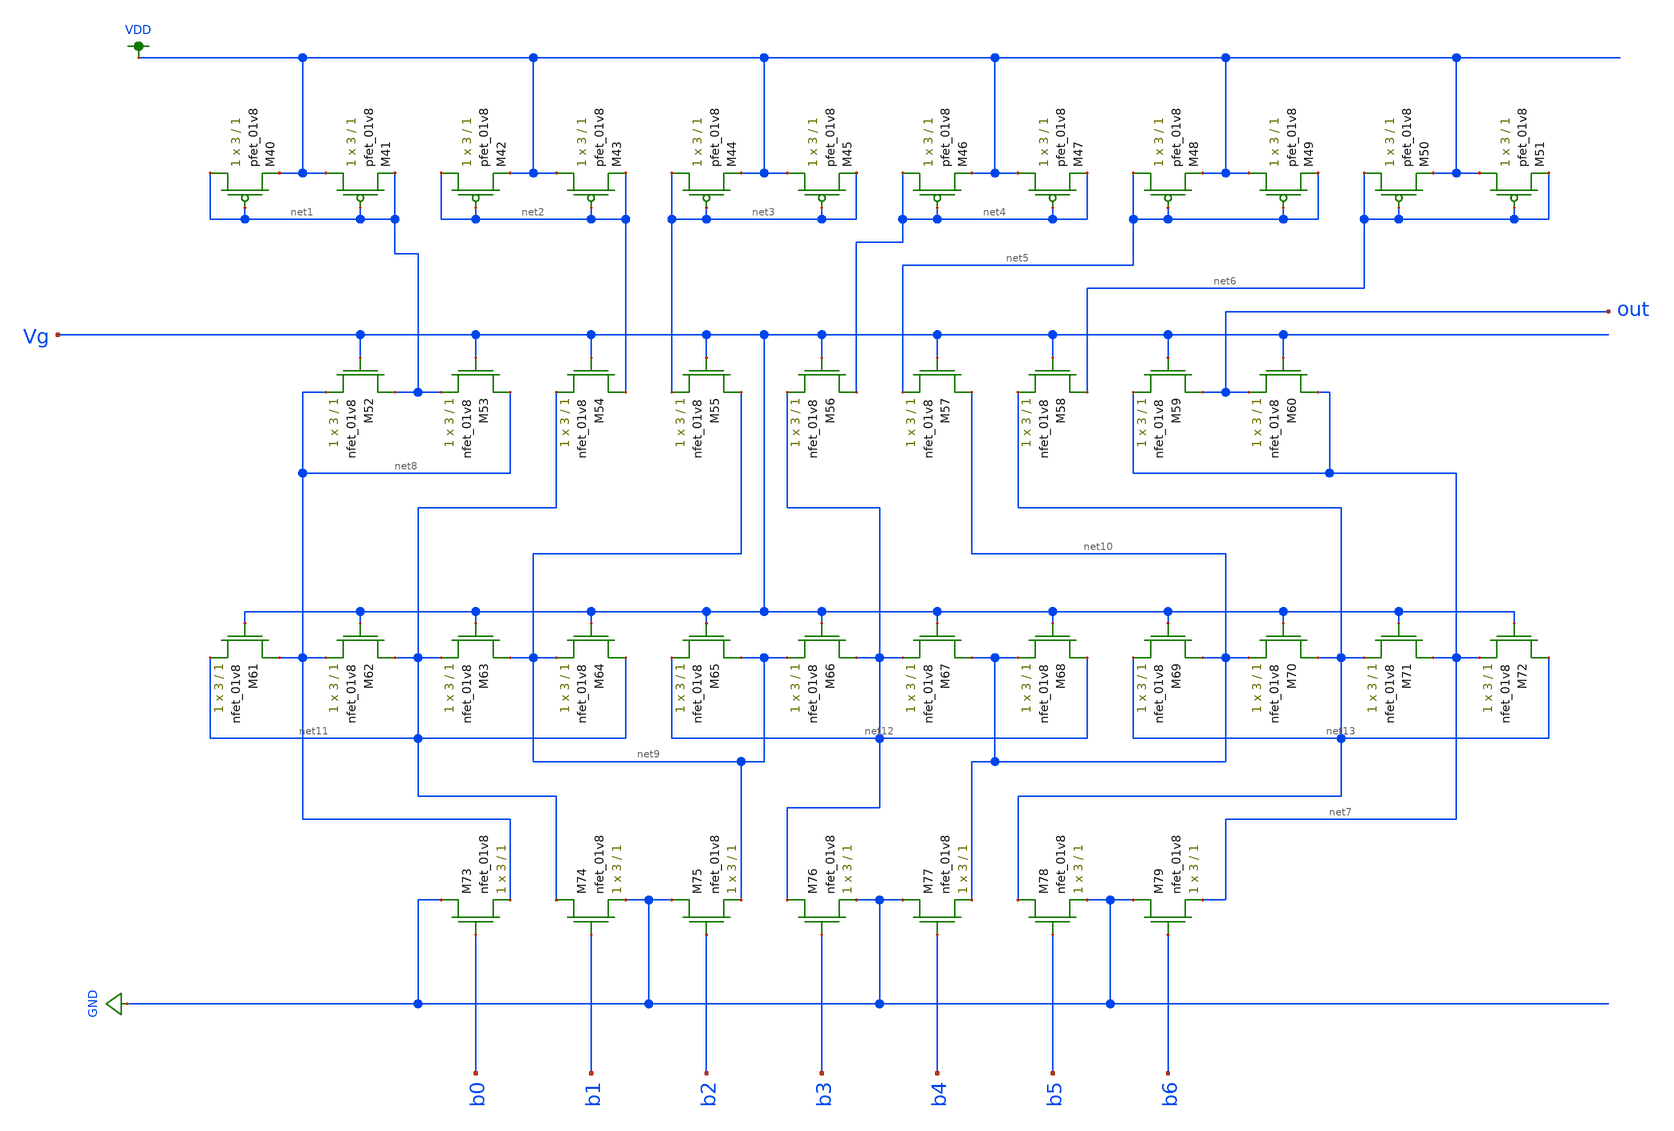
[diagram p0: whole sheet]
** sch_path: schematic/LDS/dac_7_bit_LDS.sch
**.subckt dac_7_bit_LDS
XM40 net1 net1 VDD VDD sky130_fd_pr__pfet_01v8 L=1 W=3 nf=1 ad='int((nf+1)/2) * W/nf * 0.29' as='int((nf+2)/2) * W/nf * 0.29'
+ pd='2*int((nf+1)/2) * (W/nf + 0.29)' ps='2*int((nf+2)/2) * (W/nf + 0.29)' nrd='0.29 / W' nrs='0.29 / W'
+ sa=0 sb=0 sd=0 mult=1 m=1
XM41 VDD net1 net1 VDD sky130_fd_pr__pfet_01v8 L=1 W=3 nf=1 ad='int((nf+1)/2) * W/nf * 0.29' as='int((nf+2)/2) * W/nf * 0.29'
+ pd='2*int((nf+1)/2) * (W/nf + 0.29)' ps='2*int((nf+2)/2) * (W/nf + 0.29)' nrd='0.29 / W' nrs='0.29 / W'
+ sa=0 sb=0 sd=0 mult=1 m=1
XM42 net2 net2 VDD VDD sky130_fd_pr__pfet_01v8 L=1 W=3 nf=1 ad='int((nf+1)/2) * W/nf * 0.29' as='int((nf+2)/2) * W/nf * 0.29'
+ pd='2*int((nf+1)/2) * (W/nf + 0.29)' ps='2*int((nf+2)/2) * (W/nf + 0.29)' nrd='0.29 / W' nrs='0.29 / W'
+ sa=0 sb=0 sd=0 mult=1 m=1
XM43 VDD net2 net2 VDD sky130_fd_pr__pfet_01v8 L=1 W=3 nf=1 ad='int((nf+1)/2) * W/nf * 0.29' as='int((nf+2)/2) * W/nf * 0.29'
+ pd='2*int((nf+1)/2) * (W/nf + 0.29)' ps='2*int((nf+2)/2) * (W/nf + 0.29)' nrd='0.29 / W' nrs='0.29 / W'
+ sa=0 sb=0 sd=0 mult=1 m=1
XM44 net3 net3 VDD VDD sky130_fd_pr__pfet_01v8 L=1 W=3 nf=1 ad='int((nf+1)/2) * W/nf * 0.29' as='int((nf+2)/2) * W/nf * 0.29'
+ pd='2*int((nf+1)/2) * (W/nf + 0.29)' ps='2*int((nf+2)/2) * (W/nf + 0.29)' nrd='0.29 / W' nrs='0.29 / W'
+ sa=0 sb=0 sd=0 mult=1 m=1
XM45 VDD net3 net3 VDD sky130_fd_pr__pfet_01v8 L=1 W=3 nf=1 ad='int((nf+1)/2) * W/nf * 0.29' as='int((nf+2)/2) * W/nf * 0.29'
+ pd='2*int((nf+1)/2) * (W/nf + 0.29)' ps='2*int((nf+2)/2) * (W/nf + 0.29)' nrd='0.29 / W' nrs='0.29 / W'
+ sa=0 sb=0 sd=0 mult=1 m=1
XM46 net4 net4 VDD VDD sky130_fd_pr__pfet_01v8 L=1 W=3 nf=1 ad='int((nf+1)/2) * W/nf * 0.29' as='int((nf+2)/2) * W/nf * 0.29'
+ pd='2*int((nf+1)/2) * (W/nf + 0.29)' ps='2*int((nf+2)/2) * (W/nf + 0.29)' nrd='0.29 / W' nrs='0.29 / W'
+ sa=0 sb=0 sd=0 mult=1 m=1
XM47 VDD net4 net4 VDD sky130_fd_pr__pfet_01v8 L=1 W=3 nf=1 ad='int((nf+1)/2) * W/nf * 0.29' as='int((nf+2)/2) * W/nf * 0.29'
+ pd='2*int((nf+1)/2) * (W/nf + 0.29)' ps='2*int((nf+2)/2) * (W/nf + 0.29)' nrd='0.29 / W' nrs='0.29 / W'
+ sa=0 sb=0 sd=0 mult=1 m=1
XM48 net5 net5 VDD VDD sky130_fd_pr__pfet_01v8 L=1 W=3 nf=1 ad='int((nf+1)/2) * W/nf * 0.29' as='int((nf+2)/2) * W/nf * 0.29'
+ pd='2*int((nf+1)/2) * (W/nf + 0.29)' ps='2*int((nf+2)/2) * (W/nf + 0.29)' nrd='0.29 / W' nrs='0.29 / W'
+ sa=0 sb=0 sd=0 mult=1 m=1
XM49 VDD net5 net5 VDD sky130_fd_pr__pfet_01v8 L=1 W=3 nf=1 ad='int((nf+1)/2) * W/nf * 0.29' as='int((nf+2)/2) * W/nf * 0.29'
+ pd='2*int((nf+1)/2) * (W/nf + 0.29)' ps='2*int((nf+2)/2) * (W/nf + 0.29)' nrd='0.29 / W' nrs='0.29 / W'
+ sa=0 sb=0 sd=0 mult=1 m=1
XM50 net6 net6 VDD VDD sky130_fd_pr__pfet_01v8 L=1 W=3 nf=1 ad='int((nf+1)/2) * W/nf * 0.29' as='int((nf+2)/2) * W/nf * 0.29'
+ pd='2*int((nf+1)/2) * (W/nf + 0.29)' ps='2*int((nf+2)/2) * (W/nf + 0.29)' nrd='0.29 / W' nrs='0.29 / W'
+ sa=0 sb=0 sd=0 mult=1 m=1
XM51 VDD net6 net6 VDD sky130_fd_pr__pfet_01v8 L=1 W=3 nf=1 ad='int((nf+1)/2) * W/nf * 0.29' as='int((nf+2)/2) * W/nf * 0.29'
+ pd='2*int((nf+1)/2) * (W/nf + 0.29)' ps='2*int((nf+2)/2) * (W/nf + 0.29)' nrd='0.29 / W' nrs='0.29 / W'
+ sa=0 sb=0 sd=0 mult=1 m=1
XM52 net1 Vg net8 GND sky130_fd_pr__nfet_01v8 L=1 W=3 nf=1 ad='int((nf+1)/2) * W/nf * 0.29' as='int((nf+2)/2) * W/nf * 0.29'
+ pd='2*int((nf+1)/2) * (W/nf + 0.29)' ps='2*int((nf+2)/2) * (W/nf + 0.29)' nrd='0.29 / W' nrs='0.29 / W'
+ sa=0 sb=0 sd=0 mult=1 m=1
XM53 net8 Vg net1 GND sky130_fd_pr__nfet_01v8 L=1 W=3 nf=1 ad='int((nf+1)/2) * W/nf * 0.29' as='int((nf+2)/2) * W/nf * 0.29'
+ pd='2*int((nf+1)/2) * (W/nf + 0.29)' ps='2*int((nf+2)/2) * (W/nf + 0.29)' nrd='0.29 / W' nrs='0.29 / W'
+ sa=0 sb=0 sd=0 mult=1 m=1
XM54 net2 Vg net11 GND sky130_fd_pr__nfet_01v8 L=1 W=3 nf=1 ad='int((nf+1)/2) * W/nf * 0.29' as='int((nf+2)/2) * W/nf * 0.29'
+ pd='2*int((nf+1)/2) * (W/nf + 0.29)' ps='2*int((nf+2)/2) * (W/nf + 0.29)' nrd='0.29 / W' nrs='0.29 / W'
+ sa=0 sb=0 sd=0 mult=1 m=1
XM55 net9 Vg net3 GND sky130_fd_pr__nfet_01v8 L=1 W=3 nf=1 ad='int((nf+1)/2) * W/nf * 0.29' as='int((nf+2)/2) * W/nf * 0.29'
+ pd='2*int((nf+1)/2) * (W/nf + 0.29)' ps='2*int((nf+2)/2) * (W/nf + 0.29)' nrd='0.29 / W' nrs='0.29 / W'
+ sa=0 sb=0 sd=0 mult=1 m=1
XM56 net4 Vg net12 GND sky130_fd_pr__nfet_01v8 L=1 W=3 nf=1 ad='int((nf+1)/2) * W/nf * 0.29' as='int((nf+2)/2) * W/nf * 0.29'
+ pd='2*int((nf+1)/2) * (W/nf + 0.29)' ps='2*int((nf+2)/2) * (W/nf + 0.29)' nrd='0.29 / W' nrs='0.29 / W'
+ sa=0 sb=0 sd=0 mult=1 m=1
XM57 net10 Vg net5 GND sky130_fd_pr__nfet_01v8 L=1 W=3 nf=1 ad='int((nf+1)/2) * W/nf * 0.29' as='int((nf+2)/2) * W/nf * 0.29'
+ pd='2*int((nf+1)/2) * (W/nf + 0.29)' ps='2*int((nf+2)/2) * (W/nf + 0.29)' nrd='0.29 / W' nrs='0.29 / W'
+ sa=0 sb=0 sd=0 mult=1 m=1
XM58 net6 Vg net13 GND sky130_fd_pr__nfet_01v8 L=1 W=3 nf=1 ad='int((nf+1)/2) * W/nf * 0.29' as='int((nf+2)/2) * W/nf * 0.29'
+ pd='2*int((nf+1)/2) * (W/nf + 0.29)' ps='2*int((nf+2)/2) * (W/nf + 0.29)' nrd='0.29 / W' nrs='0.29 / W'
+ sa=0 sb=0 sd=0 mult=1 m=1
XM59 out Vg net7 GND sky130_fd_pr__nfet_01v8 L=1 W=3 nf=1 ad='int((nf+1)/2) * W/nf * 0.29' as='int((nf+2)/2) * W/nf * 0.29'
+ pd='2*int((nf+1)/2) * (W/nf + 0.29)' ps='2*int((nf+2)/2) * (W/nf + 0.29)' nrd='0.29 / W' nrs='0.29 / W'
+ sa=0 sb=0 sd=0 mult=1 m=1
XM60 net7 Vg out GND sky130_fd_pr__nfet_01v8 L=1 W=3 nf=1 ad='int((nf+1)/2) * W/nf * 0.29' as='int((nf+2)/2) * W/nf * 0.29'
+ pd='2*int((nf+1)/2) * (W/nf + 0.29)' ps='2*int((nf+2)/2) * (W/nf + 0.29)' nrd='0.29 / W' nrs='0.29 / W'
+ sa=0 sb=0 sd=0 mult=1 m=1
XM61 net8 Vg net11 GND sky130_fd_pr__nfet_01v8 L=1 W=3 nf=1 ad='int((nf+1)/2) * W/nf * 0.29' as='int((nf+2)/2) * W/nf * 0.29'
+ pd='2*int((nf+1)/2) * (W/nf + 0.29)' ps='2*int((nf+2)/2) * (W/nf + 0.29)' nrd='0.29 / W' nrs='0.29 / W'
+ sa=0 sb=0 sd=0 mult=1 m=1
XM62 net11 Vg net8 GND sky130_fd_pr__nfet_01v8 L=1 W=3 nf=1 ad='int((nf+1)/2) * W/nf * 0.29' as='int((nf+2)/2) * W/nf * 0.29'
+ pd='2*int((nf+1)/2) * (W/nf + 0.29)' ps='2*int((nf+2)/2) * (W/nf + 0.29)' nrd='0.29 / W' nrs='0.29 / W'
+ sa=0 sb=0 sd=0 mult=1 m=1
XM63 net9 Vg net11 GND sky130_fd_pr__nfet_01v8 L=1 W=3 nf=1 ad='int((nf+1)/2) * W/nf * 0.29' as='int((nf+2)/2) * W/nf * 0.29'
+ pd='2*int((nf+1)/2) * (W/nf + 0.29)' ps='2*int((nf+2)/2) * (W/nf + 0.29)' nrd='0.29 / W' nrs='0.29 / W'
+ sa=0 sb=0 sd=0 mult=1 m=1
XM64 net11 Vg net9 GND sky130_fd_pr__nfet_01v8 L=1 W=3 nf=1 ad='int((nf+1)/2) * W/nf * 0.29' as='int((nf+2)/2) * W/nf * 0.29'
+ pd='2*int((nf+1)/2) * (W/nf + 0.29)' ps='2*int((nf+2)/2) * (W/nf + 0.29)' nrd='0.29 / W' nrs='0.29 / W'
+ sa=0 sb=0 sd=0 mult=1 m=1
XM65 net9 Vg net12 GND sky130_fd_pr__nfet_01v8 L=1 W=3 nf=1 ad='int((nf+1)/2) * W/nf * 0.29' as='int((nf+2)/2) * W/nf * 0.29'
+ pd='2*int((nf+1)/2) * (W/nf + 0.29)' ps='2*int((nf+2)/2) * (W/nf + 0.29)' nrd='0.29 / W' nrs='0.29 / W'
+ sa=0 sb=0 sd=0 mult=1 m=1
XM66 net12 Vg net9 GND sky130_fd_pr__nfet_01v8 L=1 W=3 nf=1 ad='int((nf+1)/2) * W/nf * 0.29' as='int((nf+2)/2) * W/nf * 0.29'
+ pd='2*int((nf+1)/2) * (W/nf + 0.29)' ps='2*int((nf+2)/2) * (W/nf + 0.29)' nrd='0.29 / W' nrs='0.29 / W'
+ sa=0 sb=0 sd=0 mult=1 m=1
XM67 net10 Vg net12 GND sky130_fd_pr__nfet_01v8 L=1 W=3 nf=1 ad='int((nf+1)/2) * W/nf * 0.29' as='int((nf+2)/2) * W/nf * 0.29'
+ pd='2*int((nf+1)/2) * (W/nf + 0.29)' ps='2*int((nf+2)/2) * (W/nf + 0.29)' nrd='0.29 / W' nrs='0.29 / W'
+ sa=0 sb=0 sd=0 mult=1 m=1
XM68 net12 Vg net10 GND sky130_fd_pr__nfet_01v8 L=1 W=3 nf=1 ad='int((nf+1)/2) * W/nf * 0.29' as='int((nf+2)/2) * W/nf * 0.29'
+ pd='2*int((nf+1)/2) * (W/nf + 0.29)' ps='2*int((nf+2)/2) * (W/nf + 0.29)' nrd='0.29 / W' nrs='0.29 / W'
+ sa=0 sb=0 sd=0 mult=1 m=1
XM69 net10 Vg net13 GND sky130_fd_pr__nfet_01v8 L=1 W=3 nf=1 ad='int((nf+1)/2) * W/nf * 0.29' as='int((nf+2)/2) * W/nf * 0.29'
+ pd='2*int((nf+1)/2) * (W/nf + 0.29)' ps='2*int((nf+2)/2) * (W/nf + 0.29)' nrd='0.29 / W' nrs='0.29 / W'
+ sa=0 sb=0 sd=0 mult=1 m=1
XM70 net13 Vg net10 GND sky130_fd_pr__nfet_01v8 L=1 W=3 nf=1 ad='int((nf+1)/2) * W/nf * 0.29' as='int((nf+2)/2) * W/nf * 0.29'
+ pd='2*int((nf+1)/2) * (W/nf + 0.29)' ps='2*int((nf+2)/2) * (W/nf + 0.29)' nrd='0.29 / W' nrs='0.29 / W'
+ sa=0 sb=0 sd=0 mult=1 m=1
XM71 net7 Vg net13 GND sky130_fd_pr__nfet_01v8 L=1 W=3 nf=1 ad='int((nf+1)/2) * W/nf * 0.29' as='int((nf+2)/2) * W/nf * 0.29'
+ pd='2*int((nf+1)/2) * (W/nf + 0.29)' ps='2*int((nf+2)/2) * (W/nf + 0.29)' nrd='0.29 / W' nrs='0.29 / W'
+ sa=0 sb=0 sd=0 mult=1 m=1
XM72 net13 Vg net7 GND sky130_fd_pr__nfet_01v8 L=1 W=3 nf=1 ad='int((nf+1)/2) * W/nf * 0.29' as='int((nf+2)/2) * W/nf * 0.29'
+ pd='2*int((nf+1)/2) * (W/nf + 0.29)' ps='2*int((nf+2)/2) * (W/nf + 0.29)' nrd='0.29 / W' nrs='0.29 / W'
+ sa=0 sb=0 sd=0 mult=1 m=1
XM73 GND b0 net8 GND sky130_fd_pr__nfet_01v8 L=1 W=3 nf=1 ad='int((nf+1)/2) * W/nf * 0.29' as='int((nf+2)/2) * W/nf * 0.29'
+ pd='2*int((nf+1)/2) * (W/nf + 0.29)' ps='2*int((nf+2)/2) * (W/nf + 0.29)' nrd='0.29 / W' nrs='0.29 / W'
+ sa=0 sb=0 sd=0 mult=1 m=1
XM74 net11 b1 GND GND sky130_fd_pr__nfet_01v8 L=1 W=3 nf=1 ad='int((nf+1)/2) * W/nf * 0.29' as='int((nf+2)/2) * W/nf * 0.29'
+ pd='2*int((nf+1)/2) * (W/nf + 0.29)' ps='2*int((nf+2)/2) * (W/nf + 0.29)' nrd='0.29 / W' nrs='0.29 / W'
+ sa=0 sb=0 sd=0 mult=1 m=1
XM75 GND b2 net9 GND sky130_fd_pr__nfet_01v8 L=1 W=3 nf=1 ad='int((nf+1)/2) * W/nf * 0.29' as='int((nf+2)/2) * W/nf * 0.29'
+ pd='2*int((nf+1)/2) * (W/nf + 0.29)' ps='2*int((nf+2)/2) * (W/nf + 0.29)' nrd='0.29 / W' nrs='0.29 / W'
+ sa=0 sb=0 sd=0 mult=1 m=1
XM76 net12 b3 GND GND sky130_fd_pr__nfet_01v8 L=1 W=3 nf=1 ad='int((nf+1)/2) * W/nf * 0.29' as='int((nf+2)/2) * W/nf * 0.29'
+ pd='2*int((nf+1)/2) * (W/nf + 0.29)' ps='2*int((nf+2)/2) * (W/nf + 0.29)' nrd='0.29 / W' nrs='0.29 / W'
+ sa=0 sb=0 sd=0 mult=1 m=1
XM77 GND b4 net10 GND sky130_fd_pr__nfet_01v8 L=1 W=3 nf=1 ad='int((nf+1)/2) * W/nf * 0.29' as='int((nf+2)/2) * W/nf * 0.29'
+ pd='2*int((nf+1)/2) * (W/nf + 0.29)' ps='2*int((nf+2)/2) * (W/nf + 0.29)' nrd='0.29 / W' nrs='0.29 / W'
+ sa=0 sb=0 sd=0 mult=1 m=1
XM78 net13 b5 GND GND sky130_fd_pr__nfet_01v8 L=1 W=3 nf=1 ad='int((nf+1)/2) * W/nf * 0.29' as='int((nf+2)/2) * W/nf * 0.29'
+ pd='2*int((nf+1)/2) * (W/nf + 0.29)' ps='2*int((nf+2)/2) * (W/nf + 0.29)' nrd='0.29 / W' nrs='0.29 / W'
+ sa=0 sb=0 sd=0 mult=1 m=1
XM79 GND b6 net7 GND sky130_fd_pr__nfet_01v8 L=1 W=3 nf=1 ad='int((nf+1)/2) * W/nf * 0.29' as='int((nf+2)/2) * W/nf * 0.29'
+ pd='2*int((nf+1)/2) * (W/nf + 0.29)' ps='2*int((nf+2)/2) * (W/nf + 0.29)' nrd='0.29 / W' nrs='0.29 / W'
+ sa=0 sb=0 sd=0 mult=1 m=1
**.ends
.GLOBAL GND
.GLOBAL VDD
.end
